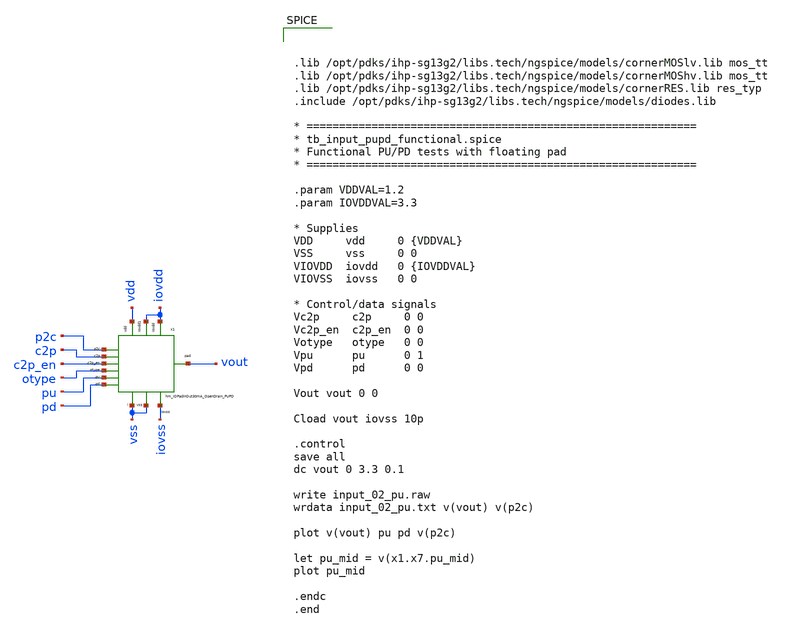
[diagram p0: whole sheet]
** sch_path: ihp-sg13g2/libs.tech/xschem/tests/tb_imodepupd_hm_IOPadInOut30mA_OpenDrain_PUPD.sch
**.subckt tb_imodepupd_hm_IOPadInOut30mA_OpenDrain_PUPD
x1 iovdd iovdd vdd pu c2p vout c2p_en pd otype p2c vss vss iovss hm_IOPadInOut30mA_OpenDrain_PUPD
**** begin user architecture code



.lib /opt/pdks/ihp-sg13g2/libs.tech/ngspice/models/cornerMOSlv.lib mos_tt
.lib /opt/pdks/ihp-sg13g2/libs.tech/ngspice/models/cornerMOShv.lib mos_tt
.lib /opt/pdks/ihp-sg13g2/libs.tech/ngspice/models/cornerRES.lib res_typ
.include /opt/pdks/ihp-sg13g2/libs.tech/ngspice/models/diodes.lib

* ============================================================
* tb_input_pupd_functional.spice
* Functional PU/PD tests with floating pad
* ============================================================

.param VDDVAL=1.2
.param IOVDDVAL=3.3

* Supplies
VDD     vdd     0 {VDDVAL}
VSS     vss     0 0
VIOVDD  iovdd   0 {IOVDDVAL}
VIOVSS  iovss   0 0

* Control/data signals
Vc2p     c2p     0 0
Vc2p_en  c2p_en  0 0
Votype   otype   0 0
Vpu      pu      0 1
Vpd      pd      0 0

Vout vout 0 0

Cload vout iovss 10p

.control
save all
dc vout 0 3.3 0.1

write input_02_pu.raw
wrdata input_02_pu.txt v(vout) v(p2c)

plot v(vout) pu pd v(p2c)

let pu_mid = v(x1.x7.pu_mid)
plot pu_mid

.endc
.end




**** end user architecture code
**.ends
.end
